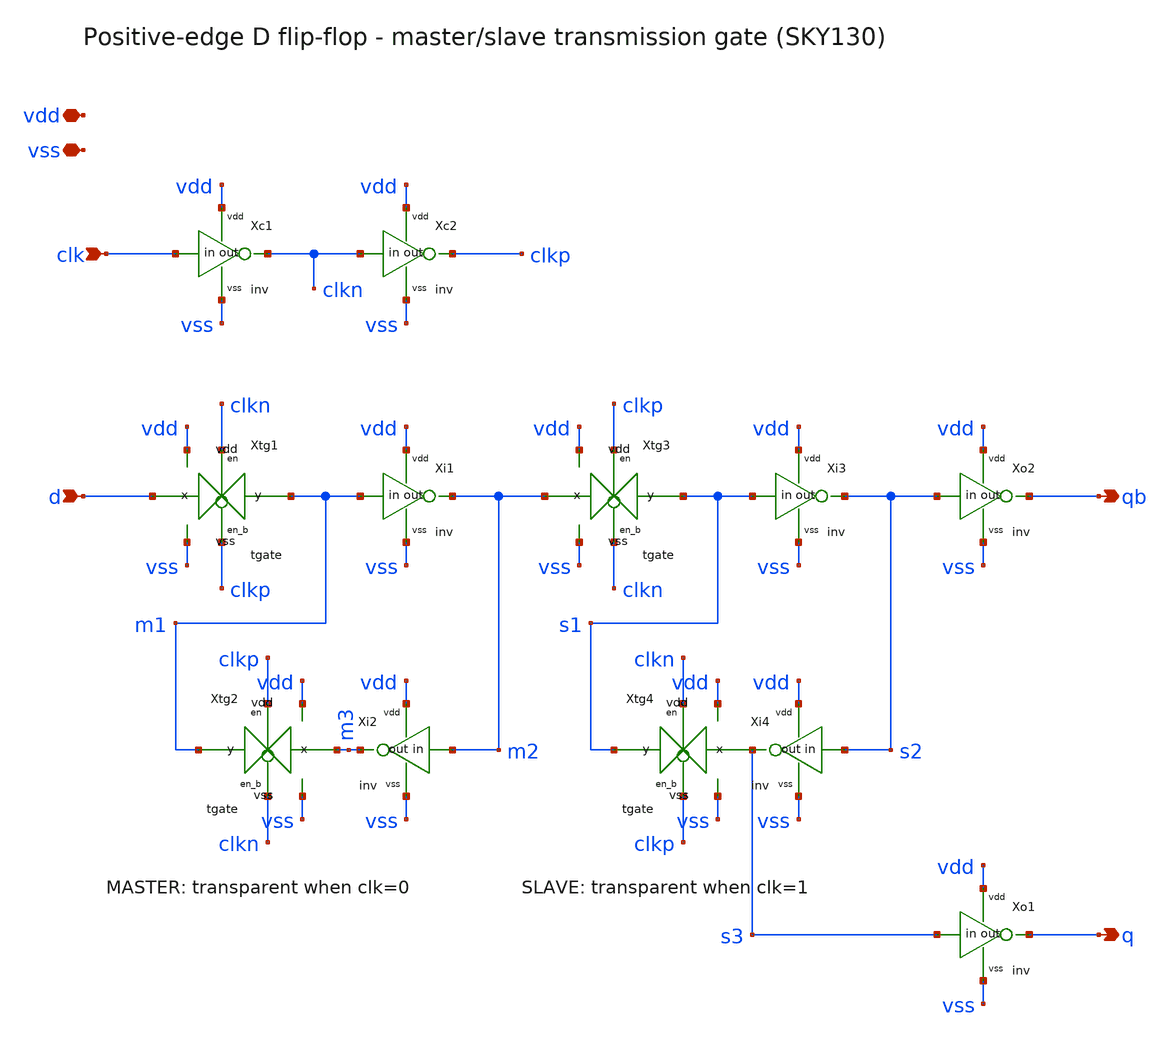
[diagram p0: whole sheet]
** sch_path: lab5/xschem/dff.sch
**.subckt dff d clk q qb vdd vss
*.ipin d
*.ipin clk
*.opin q
*.opin qb
*.iopin vdd
*.iopin vss
Xc1 clk clkn vdd vss inv
Xc2 clkn clkp vdd vss inv
Xtg1 d m1 clkn clkp vdd vss tgate
Xi1 m1 m2 vdd vss inv
Xi2 m2 m3 vdd vss inv
Xtg2 m3 m1 clkp clkn vdd vss tgate
Xtg3 m2 s1 clkp clkn vdd vss tgate
Xi3 s1 s2 vdd vss inv
Xi4 s2 s3 vdd vss inv
Xtg4 s3 s1 clkn clkp vdd vss tgate
Xo2 s2 qb vdd vss inv
Xo1 s3 q vdd vss inv
**.ends
.end
